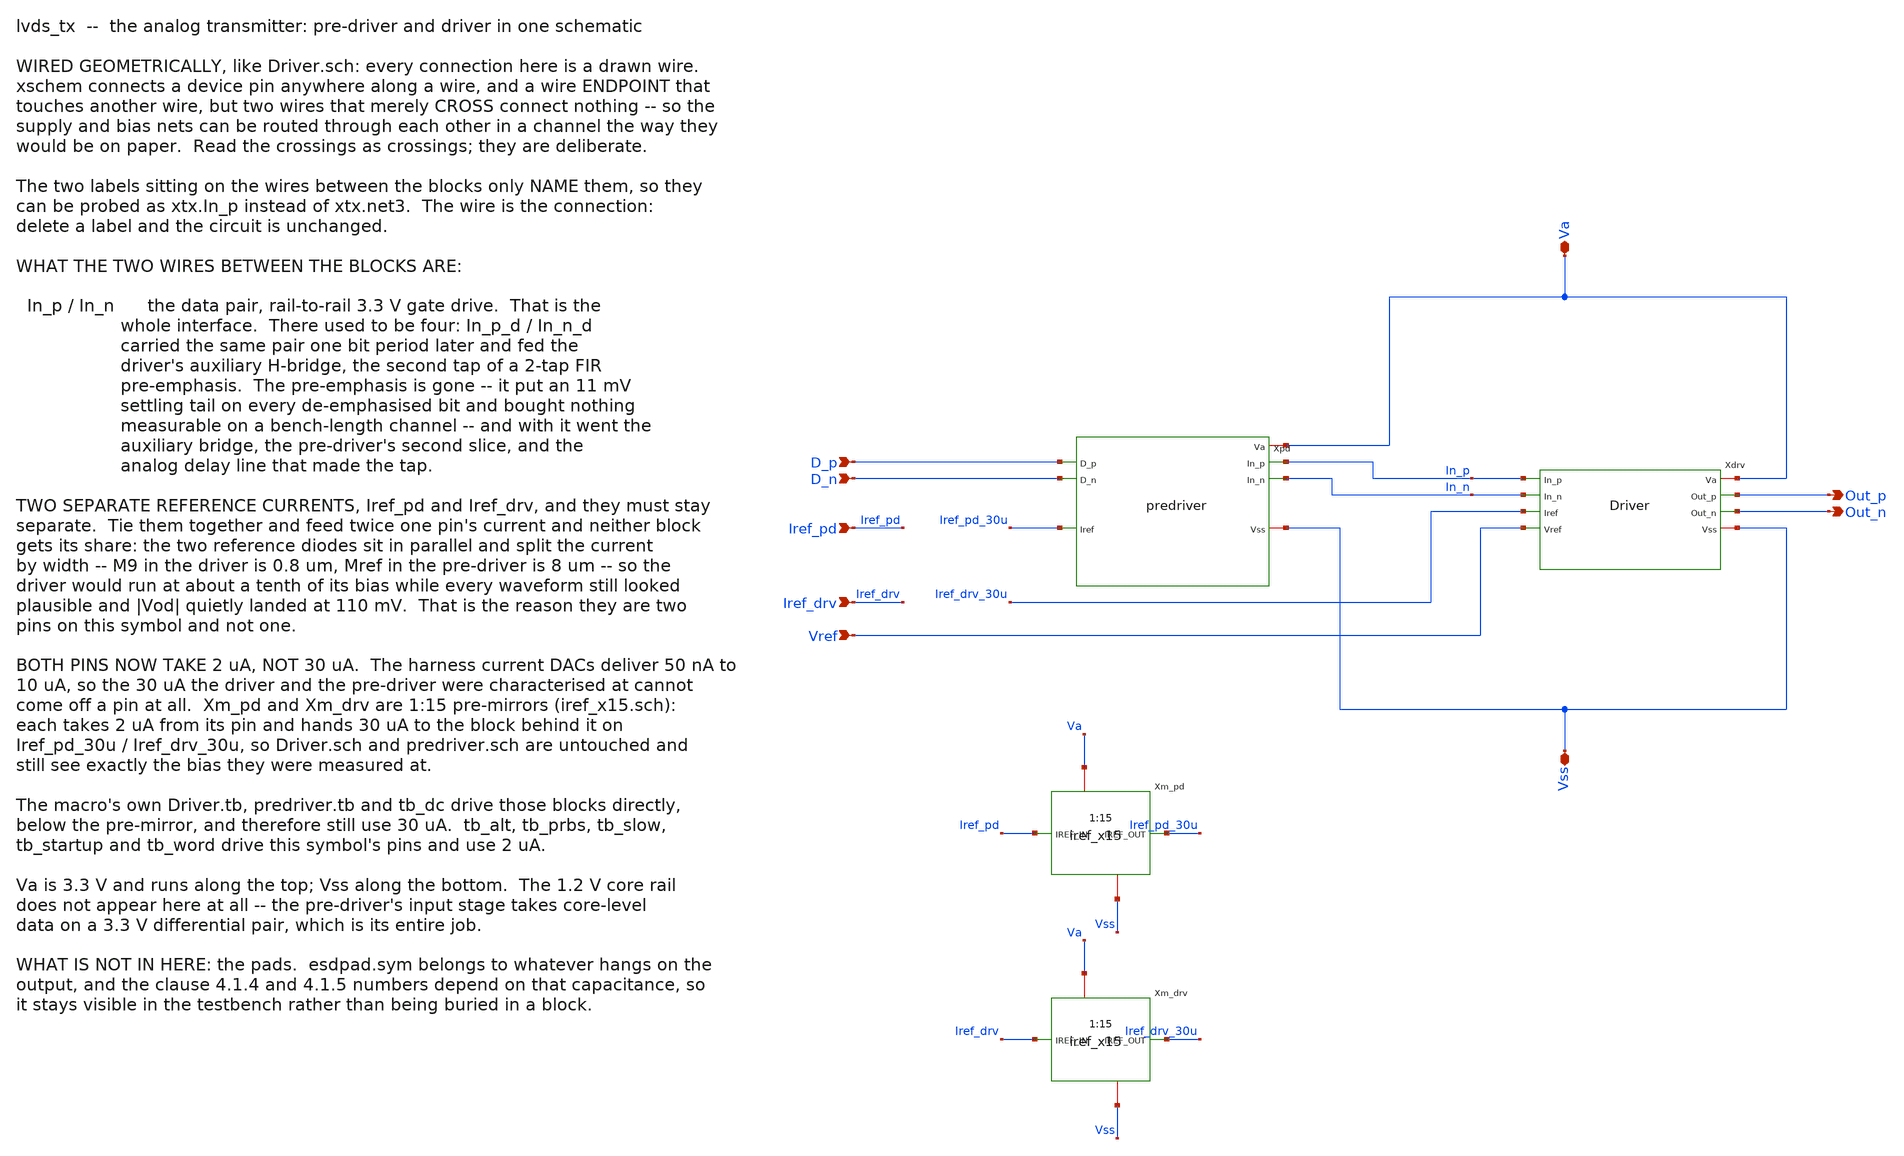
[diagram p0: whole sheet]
** sch_path: macros/lvds_tx/schematic/xschem/lvds_tx.sch
**.subckt lvds_tx D_p D_n Iref_pd Iref_drv Vref Va Vss Out_p Out_n
*.ipin D_p
*.ipin D_n
*.ipin Iref_pd
*.ipin Iref_drv
*.ipin Vref
*.iopin Va
*.iopin Vss
*.opin Out_p
*.opin Out_n
Xm_pd Iref_pd Iref_pd_30u Va Vss iref_x15
Xm_drv Iref_drv Iref_drv_30u Va Vss iref_x15
Xpd D_p D_n Iref_pd_30u In_p In_n Va Vss predriver
Xdrv Va Out_p In_p In_n Iref_drv_30u Vref Out_n Vss Driver
**.ends

* expanding   symbol:  iref_x15.sym # of pins=4
** sym_path: macros/iref_x15/schematic/xschem/iref_x15.sym
** sch_path: macros/iref_x15/schematic/xschem/iref_x15.sch
.subckt iref_x15 IREF_IN IREF_OUT Va Vss
*.ipin IREF_IN
*.opin IREF_OUT
*.iopin Va
*.iopin Vss
XMn1 IREF_IN IREF_IN Vss Vss sg13_hv_nmos w=3.2u l=2u ng=1 m=1 mm_ok=1
XMn2 CASC IREF_IN Vss Vss sg13_hv_nmos w=48u l=2u ng=6 m=1 mm_ok=1
XMp1 CASC CASC Va Va sg13_hv_pmos w=48u l=2u ng=6 m=1 mm_ok=1
XMp2 IREF_OUT CASC Va Va sg13_hv_pmos w=48u l=2u ng=6 m=1 mm_ok=1
.ends


* expanding   symbol:  predriver.sym # of pins=7
** sym_path: macros/lvds_tx/schematic/xschem/predriver.sym
** sch_path: macros/lvds_tx/schematic/xschem/predriver.sch
.subckt predriver D_p D_n Iref In_p In_n Va Vss
*.iopin Va
*.iopin Vss
*.ipin Iref
*.ipin D_p
*.ipin D_n
*.opin In_p
*.opin In_n
Xkpm D_p D_n Iref net1 Va Vss predriver_comp
XMref Iref Iref Vss Vss sg13_hv_nmos w=8u l=0.5u ng=1 m=1 mm_ok=1
Xknm D_n D_p Iref net2 Va Vss predriver_comp
Xstm net1 net2 In_p In_n Va Vss predriver_stage
.ends


* expanding   symbol:  Driver.sym # of pins=8
** sym_path: macros/lvds_tx/schematic/xschem/Driver.sym
** sch_path: macros/lvds_tx/schematic/xschem/Driver.sch
.subckt Driver Va Out_p In_p In_n Iref Vref Out_n Vss
*.iopin Va
*.iopin Vss
*.opin Out_p
*.opin Out_n
*.ipin In_p
*.ipin In_n
*.ipin Iref
*.ipin Vref
XCtn1 Va tail_n Va Va sg13_hv_pmos w=11.8u l=5.25u ng=2 m=1 mm_ok=1
XCtn2 Va tail_n Va Va sg13_hv_pmos w=5.7u l=5.8u ng=2 m=1 mm_ok=1
XM2 tail_p cmfb Va Va sg13_hv_pmos w=97.2u l=0.5u ng=20 m=1 mm_ok=1
XM5 Out_p In_p tail_p Va sg13_hv_pmos w=80u l=0.4u ng=16 m=1 mm_ok=1
XM4 Out_n In_n tail_p Va sg13_hv_pmos w=80u l=0.4u ng=16 m=1 mm_ok=1
XM1 Out_p In_p tail_n Vss sg13_hv_nmos w=30u l=0.45u ng=15 m=1 mm_ok=1
XM3 Out_n In_n tail_n Vss sg13_hv_nmos w=30u l=0.45u ng=15 m=1 mm_ok=1
XM6 tail_n Iref Vss Vss sg13_hv_nmos w=49.6u l=0.5u ng=31 m=2 mm_ok=1
XM9 Iref Iref Vss Vss sg13_hv_nmos w=0.8u l=0.5u ng=1 m=1 mm_ok=1
XM13 pd pd Va Va sg13_hv_pmos w=5u l=1u ng=1 m=1 mm_ok=1
XM14 cmfb pd Va Va sg13_hv_pmos w=5u l=1u ng=1 m=1 mm_ok=1
XM11 pd cm otail Vss sg13_hv_nmos w=40u l=1u ng=16 m=1 mm_ok=1
XM12 cmfb Vref otail Vss sg13_hv_nmos w=40u l=1u ng=16 m=1 mm_ok=1
XM10 otail Iref Vss Vss sg13_hv_nmos w=0.8u l=0.5u ng=1 m=1 mm_ok=1
XCc Va cc_g Va Va sg13_hv_pmos w=50u l=5u ng=10 m=1 mm_ok=1
XRc cmfb cc_g Vss rppd w=1u l=6u m=1 b=0 mm_ok=1
XRp Out_p cm Vss rhigh w=1u l=7.35u m=1 b=0 mm_ok=1
XRn Out_n cm Vss rhigh w=1u l=7.35u m=1 b=0 mm_ok=1
XCxp Out_p In_n cap_cmomf w=5.913u l=5.913u mmin=1 mmax=4 subblock=0 rfmodel=0 subscale=1 m=1
+ mm_ok=1
XCxn Out_n In_p cap_cmomf w=5.913u l=5.913u mmin=1 mmax=4 subblock=0 rfmodel=0 subscale=1 m=1
+ mm_ok=1
XCop Vss Out_p Vss Vss sg13_hv_nmos w=10u l=5u ng=1 m=2 mm_ok=1
XCon Vss Out_n Vss Vss sg13_hv_nmos w=10u l=5u ng=1 m=2 mm_ok=1
.ends


* expanding   symbol:  predriver_comp.sym # of pins=6
** sym_path: macros/lvds_tx/schematic/xschem/predriver_comp.sym
** sch_path: macros/lvds_tx/schematic/xschem/predriver_comp.sch
.subckt predriver_comp Gin Din Iref Out Va Vss
*.iopin Va
*.iopin Vss
*.opin Out
*.ipin Din
*.ipin Gin
*.ipin Iref
XMld net1 net1 Va Va sg13_hv_pmos w=12u l=0.4u ng=4 m=1 mm_ok=1
XMlo Out net1 Va Va sg13_hv_pmos w=12u l=0.4u ng=4 m=1 mm_ok=1
XMid net1 Din net2 Vss sg13_hv_nmos w=24u l=0.45u ng=6 m=1 mm_ok=1
XMio Out Gin net2 Vss sg13_hv_nmos w=24u l=0.45u ng=6 m=1 mm_ok=1
XMt net2 Iref Vss Vss sg13_hv_nmos w=17.52u l=0.45u ng=6 m=2 mm_ok=1
.ends


* expanding   symbol:  predriver_stage.sym # of pins=6
** sym_path: macros/lvds_tx/schematic/xschem/predriver_stage.sym
** sch_path: macros/lvds_tx/schematic/xschem/predriver_stage.sch
.subckt predriver_stage In_p In_n Out_p Out_n Va Vss
*.ipin In_p
*.opin Out_p
*.ipin In_n
*.opin Out_n
*.iopin Va
*.iopin Vss
XMpp0 net1 In_p Va Va sg13_hv_pmos w=2.64u l=0.4u ng=1 m=1 mm_ok=1
XMnp0 net1 In_p Vss Vss sg13_hv_nmos w=1.6u l=0.45u ng=1 m=1 mm_ok=1
XMpp1 net2 net1 Va Va sg13_hv_pmos w=12.52u l=0.4u ng=4 m=1 mm_ok=1
XMnp1 net2 net1 Vss Vss sg13_hv_nmos w=5u l=0.45u ng=4 m=1 mm_ok=1
XMpp2 Out_p net2 Va Va sg13_hv_pmos w=40u l=0.4u ng=10 m=1 mm_ok=1
XMnp2 Out_p net2 Vss Vss sg13_hv_nmos w=16u l=0.45u ng=10 m=1 mm_ok=1
XMpn0 net3 In_n Va Va sg13_hv_pmos w=2.64u l=0.4u ng=1 m=1 mm_ok=1
XMnn0 net3 In_n Vss Vss sg13_hv_nmos w=1.6u l=0.45u ng=1 m=1 mm_ok=1
XMpn1 net4 net3 Va Va sg13_hv_pmos w=12.52u l=0.4u ng=4 m=1 mm_ok=1
XMnn1 net4 net3 Vss Vss sg13_hv_nmos w=5u l=0.45u ng=4 m=1 mm_ok=1
XMpn2 Out_n net4 Va Va sg13_hv_pmos w=40u l=0.4u ng=10 m=1 mm_ok=1
XMnn2 Out_n net4 Vss Vss sg13_hv_nmos w=16u l=0.45u ng=10 m=1 mm_ok=1
XMpxp net4 net2 Va Va sg13_hv_pmos w=4.38u l=0.4u ng=1 m=1 mm_ok=1
XMnxp net4 net2 Vss Vss sg13_hv_nmos w=1.75u l=0.45u ng=1 m=1 mm_ok=1
XMpxn net2 net4 Va Va sg13_hv_pmos w=4.38u l=0.4u ng=1 m=1 mm_ok=1
XMnxn net2 net4 Vss Vss sg13_hv_nmos w=1.75u l=0.45u ng=1 m=1 mm_ok=1
.ends

.end
